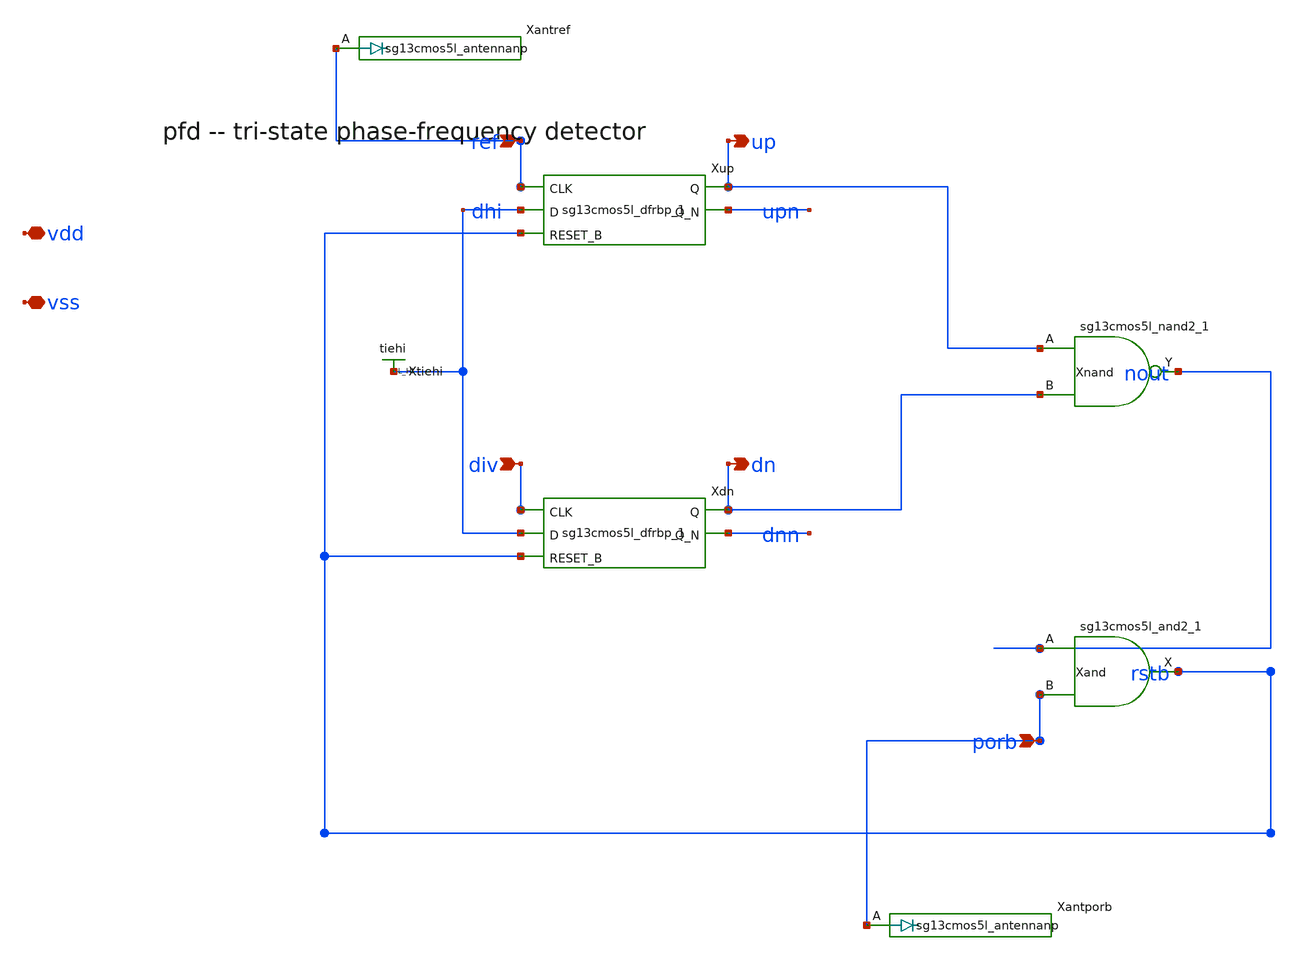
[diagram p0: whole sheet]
** sch_path: xschem/pfd_wired.sch
**.subckt pfd_wired ref div porb up dn vdd vss
*.ipin ref
*.ipin div
*.ipin porb
*.opin up
*.opin dn
*.iopin vdd
*.iopin vss
Xup up upn ref dhi rstb vdd vss sg13cmos5l_dfrbp_1
Xdn dn dnn div dhi rstb vdd vss sg13cmos5l_dfrbp_1
Xtiehi dhi vdd vss sg13cmos5l_tiehi
Xnand nout up dn vdd vss sg13cmos5l_nand2_1
Xand rstb nout porb vdd vss sg13cmos5l_and2_1
Xantref ref vdd vss sg13cmos5l_antennanp
Xantporb porb vdd vss sg13cmos5l_antennanp
**.ends
.end
